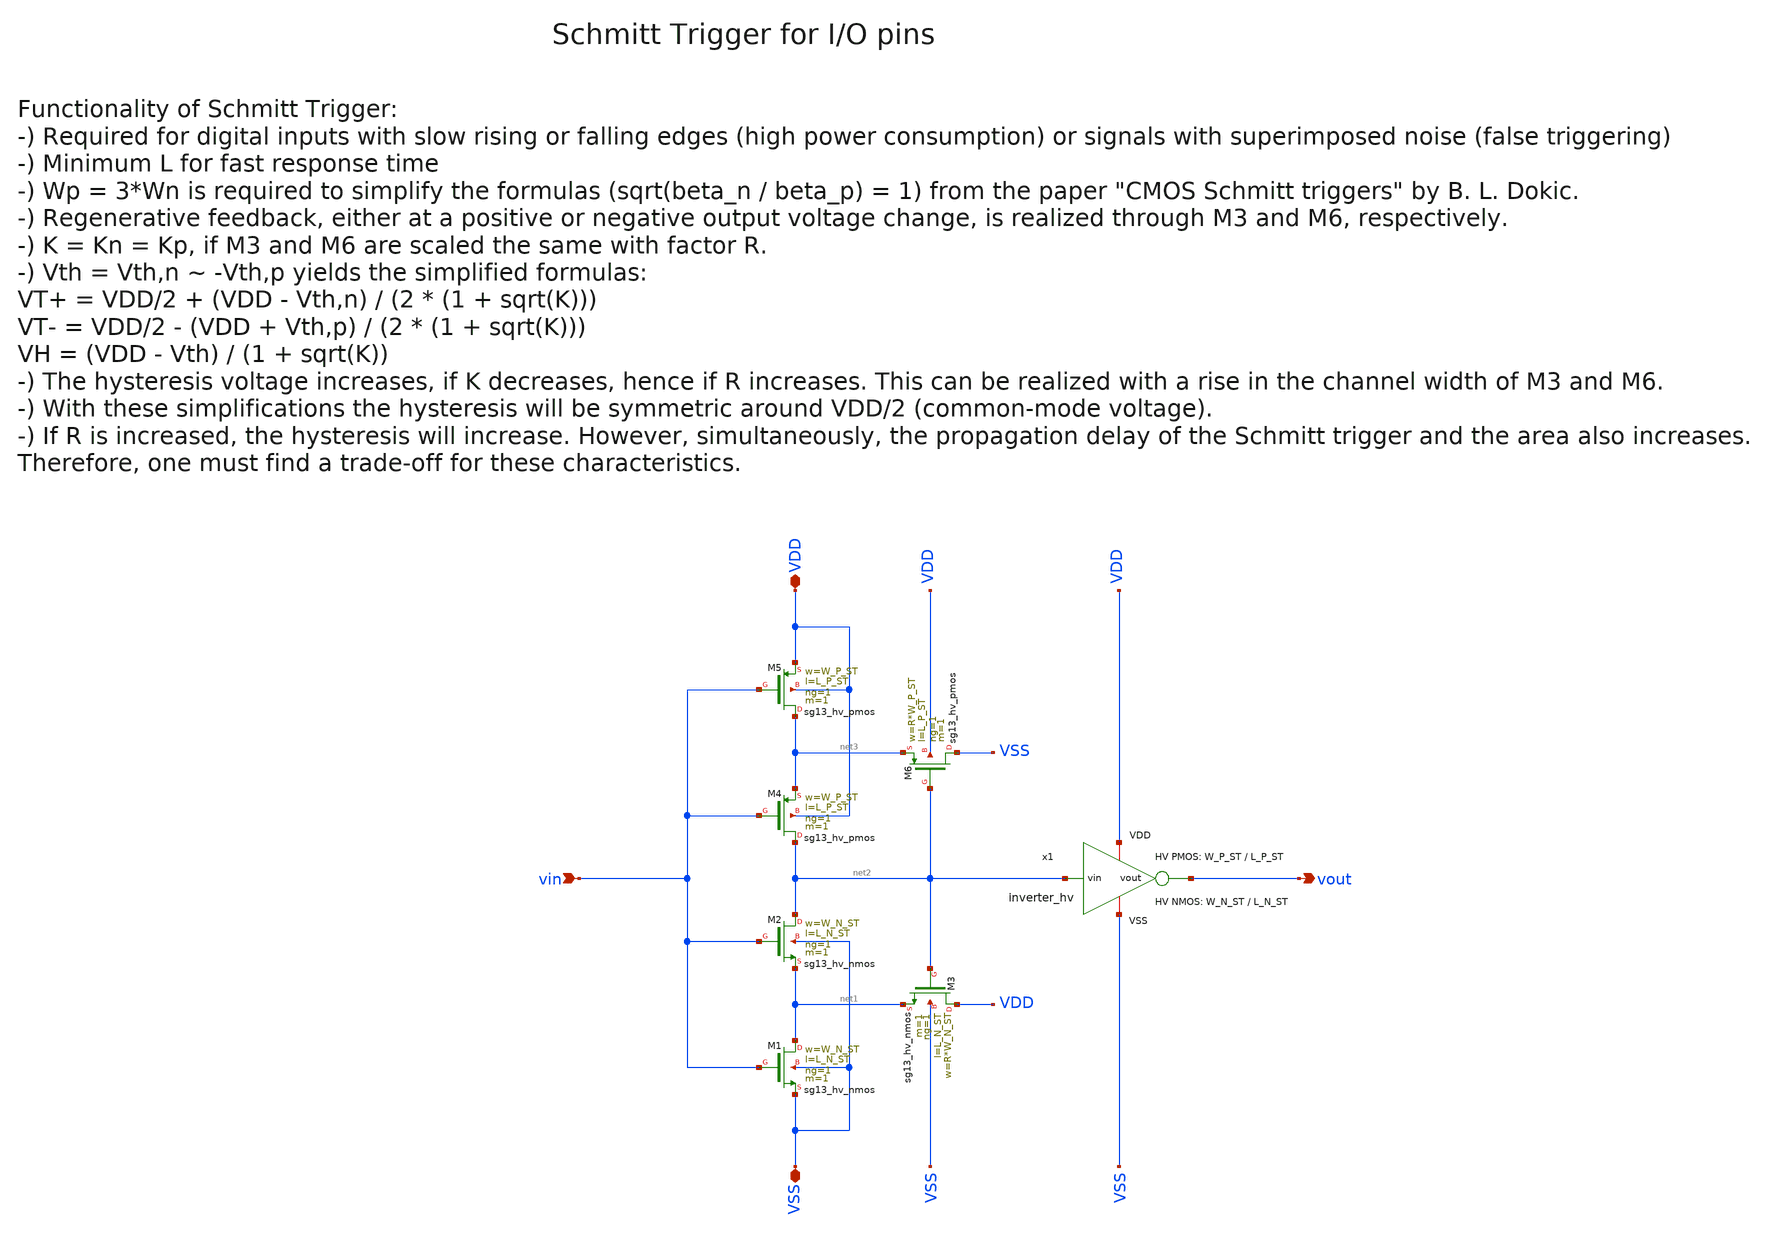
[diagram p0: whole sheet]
** sch_path: SG13G2_ATBS-ADC-main/xschem/schmitt_trigger/schmitt_trigger.sch
**.subckt schmitt_trigger VDD vout VSS vin
*.iopin VDD
*.opin vout
*.iopin VSS
*.ipin vin
x1 VDD net2 vout VSS inverter_hv W_P=W_P_ST L_P=L_P_ST W_N=W_N_ST L_N=L_N_ST
XM5 net3 vin VDD VDD sg13_hv_pmos w=W_P_ST l=L_P_ST ng=1 m=1 mm_ok=1
XM4 net2 vin net3 VDD sg13_hv_pmos w=W_P_ST l=L_P_ST ng=1 m=1 mm_ok=1
XM6 VSS net2 net3 VDD sg13_hv_pmos w=R*W_P_ST l=L_P_ST ng=1 m=1 mm_ok=1
XM1 net1 vin VSS VSS sg13_hv_nmos w=W_N_ST l=L_N_ST ng=1 m=1 mm_ok=1
XM2 net2 vin net1 VSS sg13_hv_nmos w=W_N_ST l=L_N_ST ng=1 m=1 mm_ok=1
XM3 VDD net2 net1 VSS sg13_hv_nmos w=R*W_N_ST l=L_N_ST ng=1 m=1 mm_ok=1
**.ends

* expanding   symbol:  inverter/inverter_hv.sym # of pins=4
** sym_path: SG13G2_ATBS-ADC-main/xschem/inverter/inverter_hv.sym
** sch_path: SG13G2_ATBS-ADC-main/xschem/inverter/inverter_hv.sch
.subckt inverter_hv VDD vin vout VSS  W_P=3.0u L_P=0.50u W_N=1.0u L_N=0.50u
*.ipin vin
*.iopin VDD
*.iopin VSS
*.opin vout
XM1 vout vin VDD VDD sg13_hv_pmos w=W_P l=L_P ng=1 m=1 mm_ok=1
XM2 vout vin VSS VSS sg13_hv_nmos w=W_N l=L_N ng=1 m=1 mm_ok=1
.ends

.end
